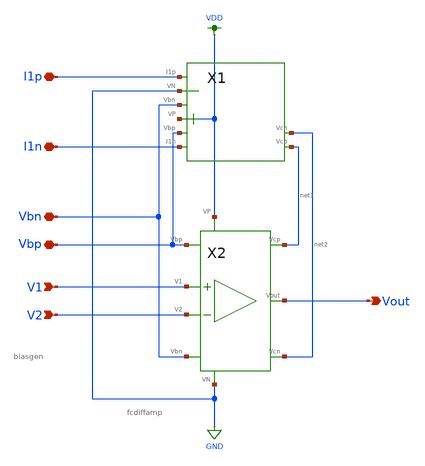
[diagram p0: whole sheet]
** sch_path: full_fcdiff.sch
**.subckt full_fcdiff V2 V1 I1p I1n Vbn Vbp Vout
*.ipin V2
*.ipin V1
*.iopin I1p
*.iopin I1n
*.iopin Vbn
*.iopin Vbp
*.opin Vout
X1 I1n Vbp VDD Vbn GND I1p net1 net2 biasgen
X2 Vbp V1 V2 Vbn GND net2 net1 VDD Vout fcdiffamp
**.ends
.GLOBAL VDD
.GLOBAL GND
.end
